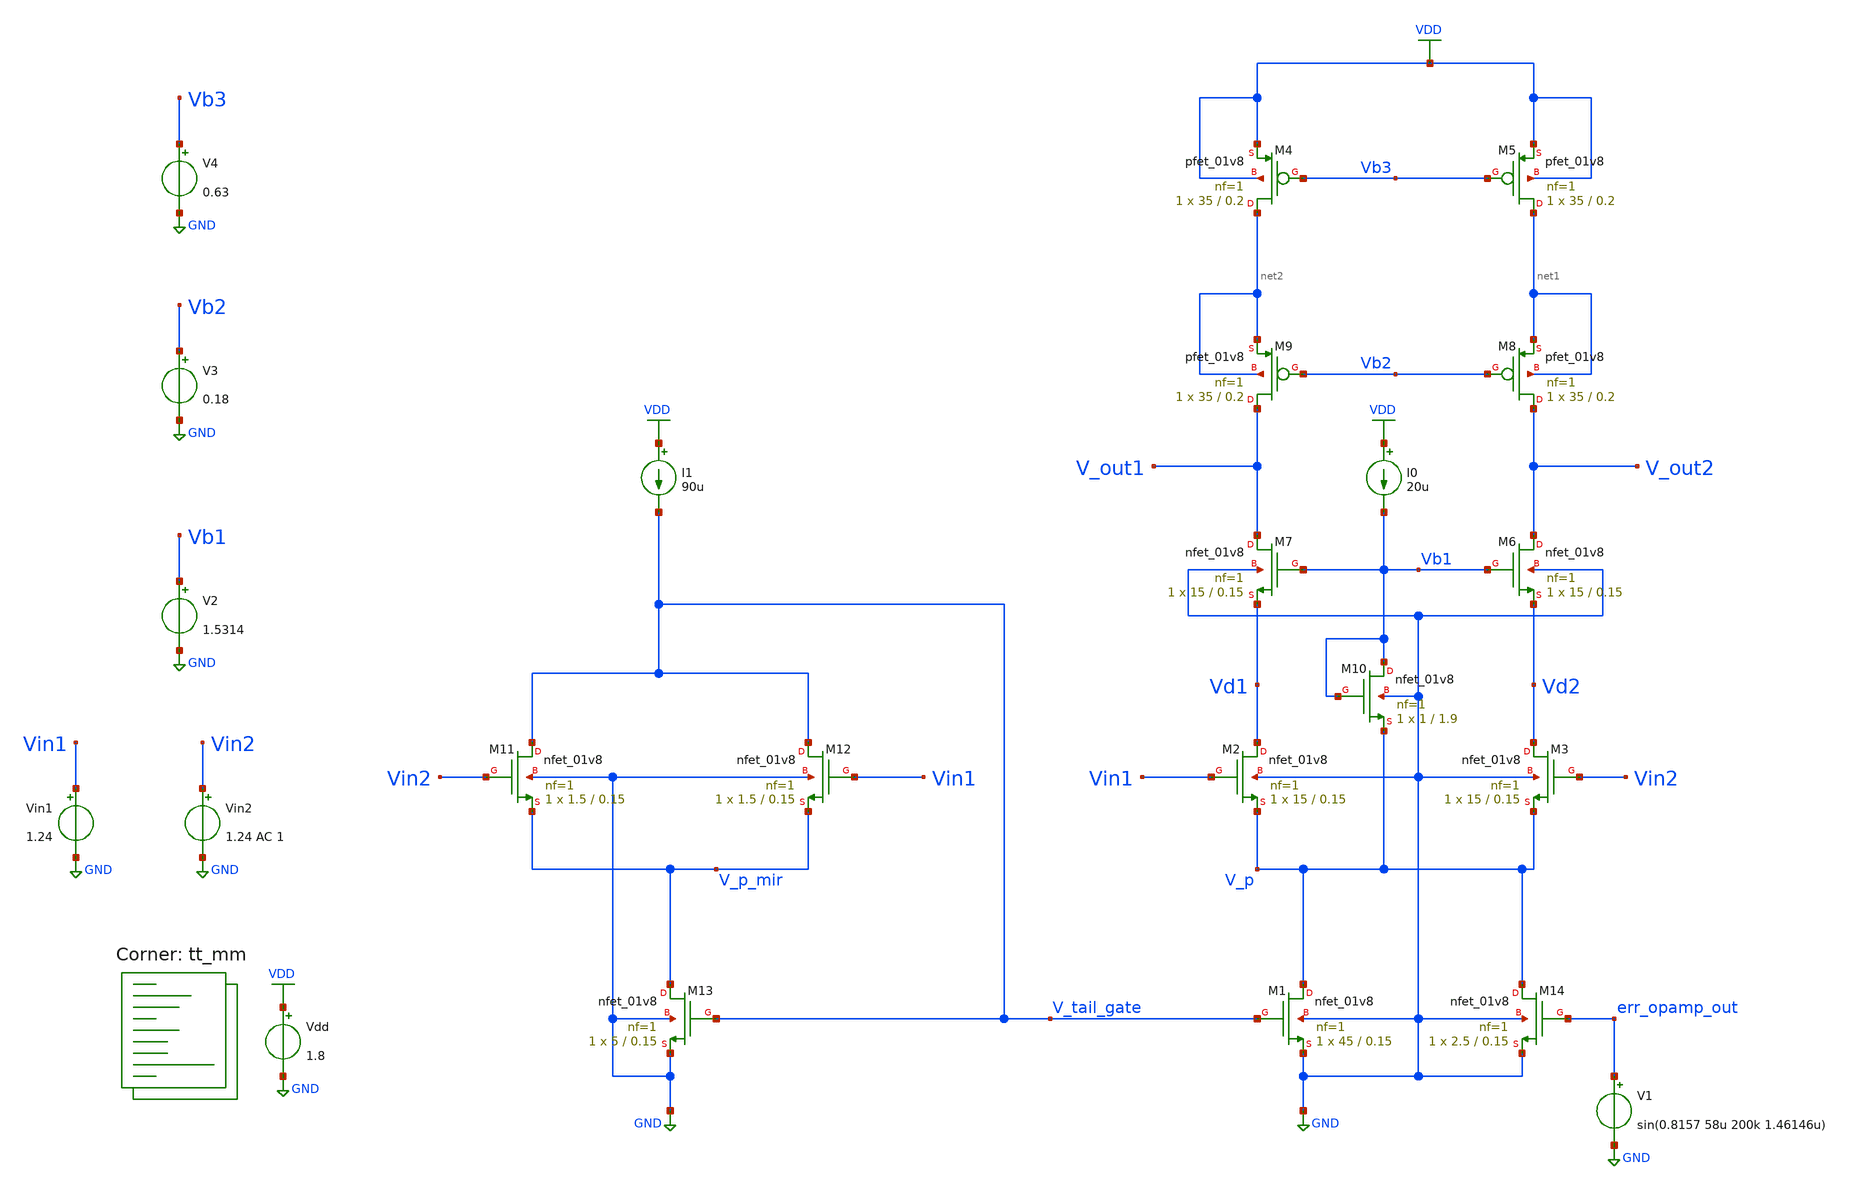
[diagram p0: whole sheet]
** sch_path: projects/montecarlo/xschem_ngspice/inverter/tb_opamp_mc.sch
**.subckt tb_opamp_mc
Vdd VDD GND 1.8
Vin1 Vin1 GND 1.24
Vin2 Vin2 GND 1.24 AC 1
XM5 net1 Vb3 VDD VDD sky130_fd_pr__pfet_01v8 L=0.2 W=35 nf=1 ad='int((nf+1)/2) * W/nf * 0.29' as='int((nf+2)/2) * W/nf * 0.29'
+ pd='2*int((nf+1)/2) * (W/nf + 0.29)' ps='2*int((nf+2)/2) * (W/nf + 0.29)' nrd='0.29 / W' nrs='0.29 / W'
+ sa=0 sb=0 sd=0 mult=1 m=1
XM4 net2 Vb3 VDD VDD sky130_fd_pr__pfet_01v8 L=0.2 W=35 nf=1 ad='int((nf+1)/2) * W/nf * 0.29' as='int((nf+2)/2) * W/nf * 0.29'
+ pd='2*int((nf+1)/2) * (W/nf + 0.29)' ps='2*int((nf+2)/2) * (W/nf + 0.29)' nrd='0.29 / W' nrs='0.29 / W'
+ sa=0 sb=0 sd=0 mult=1 m=1
XM3 Vd2 Vin2 V_p GND sky130_fd_pr__nfet_01v8 L=0.15 W=15 nf=1 ad='int((nf+1)/2) * W/nf * 0.29' as='int((nf+2)/2) * W/nf * 0.29'
+ pd='2*int((nf+1)/2) * (W/nf + 0.29)' ps='2*int((nf+2)/2) * (W/nf + 0.29)' nrd='0.29 / W' nrs='0.29 / W'
+ sa=0 sb=0 sd=0 mult=1 m=1
XM2 Vd1 Vin1 V_p GND sky130_fd_pr__nfet_01v8 L=0.15 W=15 nf=1 ad='int((nf+1)/2) * W/nf * 0.29' as='int((nf+2)/2) * W/nf * 0.29'
+ pd='2*int((nf+1)/2) * (W/nf + 0.29)' ps='2*int((nf+2)/2) * (W/nf + 0.29)' nrd='0.29 / W' nrs='0.29 / W'
+ sa=0 sb=0 sd=0 mult=1 m=1
XM1 V_p V_tail_gate GND GND sky130_fd_pr__nfet_01v8 L=0.15 W=45 nf=1 ad='int((nf+1)/2) * W/nf * 0.29'
+ as='int((nf+2)/2) * W/nf * 0.29' pd='2*int((nf+1)/2) * (W/nf + 0.29)' ps='2*int((nf+2)/2) * (W/nf + 0.29)'
+ nrd='0.29 / W' nrs='0.29 / W' sa=0 sb=0 sd=0 mult=1 m=1
XM6 V_out2 Vb1 Vd2 GND sky130_fd_pr__nfet_01v8 L=0.15 W=15 nf=1 ad='int((nf+1)/2) * W/nf * 0.29' as='int((nf+2)/2) * W/nf * 0.29'
+ pd='2*int((nf+1)/2) * (W/nf + 0.29)' ps='2*int((nf+2)/2) * (W/nf + 0.29)' nrd='0.29 / W' nrs='0.29 / W'
+ sa=0 sb=0 sd=0 mult=1 m=1
XM7 V_out1 Vb1 Vd1 GND sky130_fd_pr__nfet_01v8 L=0.15 W=15 nf=1 ad='int((nf+1)/2) * W/nf * 0.29' as='int((nf+2)/2) * W/nf * 0.29'
+ pd='2*int((nf+1)/2) * (W/nf + 0.29)' ps='2*int((nf+2)/2) * (W/nf + 0.29)' nrd='0.29 / W' nrs='0.29 / W'
+ sa=0 sb=0 sd=0 mult=1 m=1
XM8 V_out2 Vb2 net1 net1 sky130_fd_pr__pfet_01v8 L=0.2 W=35 nf=1 ad='int((nf+1)/2) * W/nf * 0.29' as='int((nf+2)/2) * W/nf * 0.29'
+ pd='2*int((nf+1)/2) * (W/nf + 0.29)' ps='2*int((nf+2)/2) * (W/nf + 0.29)' nrd='0.29 / W' nrs='0.29 / W'
+ sa=0 sb=0 sd=0 mult=1 m=1
XM9 V_out1 Vb2 net2 net2 sky130_fd_pr__pfet_01v8 L=0.2 W=35 nf=1 ad='int((nf+1)/2) * W/nf * 0.29' as='int((nf+2)/2) * W/nf * 0.29'
+ pd='2*int((nf+1)/2) * (W/nf + 0.29)' ps='2*int((nf+2)/2) * (W/nf + 0.29)' nrd='0.29 / W' nrs='0.29 / W'
+ sa=0 sb=0 sd=0 mult=1 m=1
V2 Vb1 GND 1.5314
V3 Vb2 GND 0.18
V4 Vb3 GND 0.63
I0 VDD Vb1 20u
XM10 Vb1 Vb1 V_p GND sky130_fd_pr__nfet_01v8 L=1.9 W=1 nf=1 ad='int((nf+1)/2) * W/nf * 0.29' as='int((nf+2)/2) * W/nf * 0.29'
+ pd='2*int((nf+1)/2) * (W/nf + 0.29)' ps='2*int((nf+2)/2) * (W/nf + 0.29)' nrd='0.29 / W' nrs='0.29 / W'
+ sa=0 sb=0 sd=0 mult=1 m=1
XM11 V_tail_gate Vin2 V_p_mir GND sky130_fd_pr__nfet_01v8 L=0.15 W=1.5 nf=1 ad='int((nf+1)/2) * W/nf * 0.29'
+ as='int((nf+2)/2) * W/nf * 0.29' pd='2*int((nf+1)/2) * (W/nf + 0.29)' ps='2*int((nf+2)/2) * (W/nf + 0.29)'
+ nrd='0.29 / W' nrs='0.29 / W' sa=0 sb=0 sd=0 mult=1 m=1
XM12 V_tail_gate Vin1 V_p_mir GND sky130_fd_pr__nfet_01v8 L=0.15 W=1.5 nf=1 ad='int((nf+1)/2) * W/nf * 0.29'
+ as='int((nf+2)/2) * W/nf * 0.29' pd='2*int((nf+1)/2) * (W/nf + 0.29)' ps='2*int((nf+2)/2) * (W/nf + 0.29)'
+ nrd='0.29 / W' nrs='0.29 / W' sa=0 sb=0 sd=0 mult=1 m=1
XM13 V_p_mir V_tail_gate GND GND sky130_fd_pr__nfet_01v8 L=0.15 W=5 nf=1 ad='int((nf+1)/2) * W/nf * 0.29'
+ as='int((nf+2)/2) * W/nf * 0.29' pd='2*int((nf+1)/2) * (W/nf + 0.29)' ps='2*int((nf+2)/2) * (W/nf + 0.29)'
+ nrd='0.29 / W' nrs='0.29 / W' sa=0 sb=0 sd=0 mult=1 m=1
I1 VDD V_tail_gate 90u
XM14 V_p err_opamp_out GND GND sky130_fd_pr__nfet_01v8 L=0.15 W=2.5 nf=1 ad='int((nf+1)/2) * W/nf * 0.29'
+ as='int((nf+2)/2) * W/nf * 0.29' pd='2*int((nf+1)/2) * (W/nf + 0.29)' ps='2*int((nf+2)/2) * (W/nf + 0.29)'
+ nrd='0.29 / W' nrs='0.29 / W' sa=0 sb=0 sd=0 mult=1 m=1
V1 err_opamp_out GND sin(0.8157 58u 200k 1.46146u)
**** begin user architecture code



.option wnflag=1
.option savecurrents
.save @m.xm1.msky130_fd_pr__nfet_01v8[gm] @m.xm1.msky130_fd_pr__nfet_01v8[vth] @m.xm2.msky130_fd_pr__nfet_01v8[gm] @m.xm2.msky130_fd_pr__nfet_01v8[vth] @m.xm3.msky130_fd_pr__nfet_01v8[gm] @m.xm3.msky130_fd_pr__nfet_01v8[vth] @m.xm4.msky130_fd_pr__pfet_01v8[gm] @m.xm4.msky130_fd_pr__pfet_01v8[vth] @m.xm5.msky130_fd_pr__pfet_01v8[gm] @m.xm5.msky130_fd_pr__pfet_01v8[vth] @m.xm6.msky130_fd_pr__nfet_01v8[gm] @m.xm6.msky130_fd_pr__nfet_01v8[vth] @m.xm7.msky130_fd_pr__nfet_01v8[gm] @m.xm7.msky130_fd_pr__nfet_01v8[vth] @m.xm8.msky130_fd_pr__pfet_01v8[gm] @m.xm8.msky130_fd_pr__pfet_01v8[vth] @m.xm9.msky130_fd_pr__pfet_01v8[gm] @m.xm9.msky130_fd_pr__pfet_01v8[vth] @m.xm10.msky130_fd_pr__nfet_01v8[gm] @m.xm10.msky130_fd_pr__nfet_01v8[vth]

.control

  let runs=20
  let run=1

  dowhile run <= runs
    save all
    * dc vin 0 1.8 0.01
    ac dec 20 1 1T
    * tran 1u 3m
    write tb_opamp_mc.raw
    set appendwrite
    reset
    let run = run + 1
  end

.endc



.lib $::SKYWATER_MODELS/sky130.lib.spice tt_mm
**** end user architecture code
**.ends
.GLOBAL GND
.GLOBAL VDD
.end
